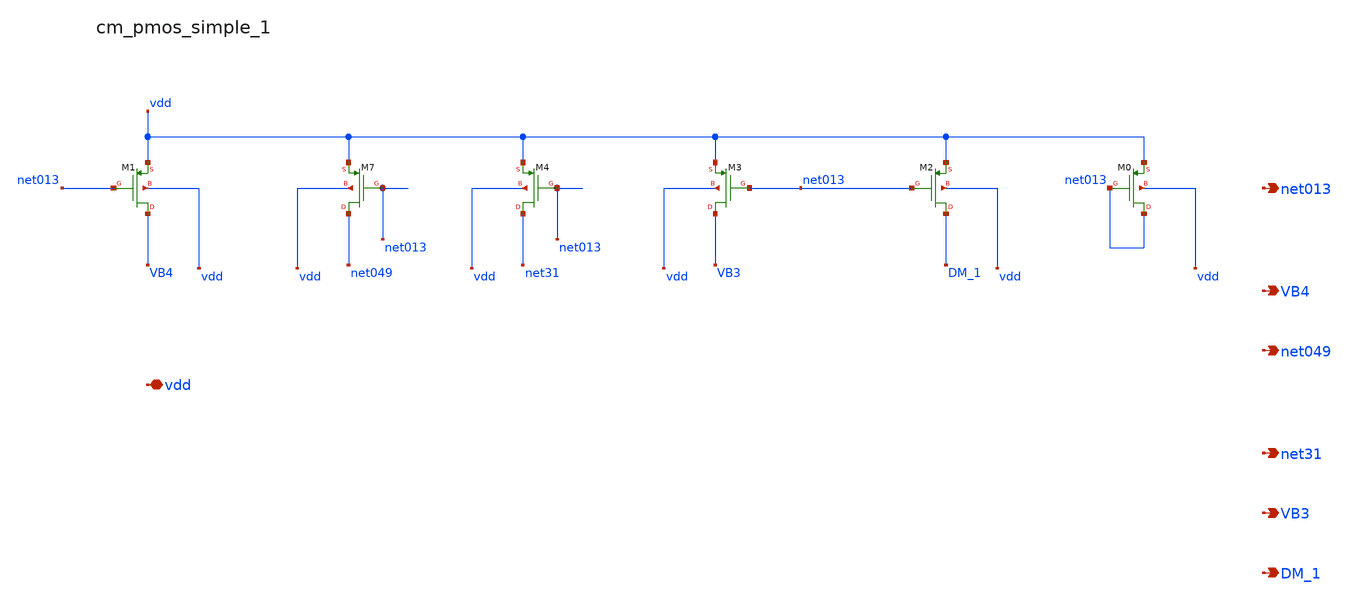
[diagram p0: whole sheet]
** sch_path: analog-db/raw/amp_008_leung_nmcf/hier/blocks/cm_pmos_simple_1.sch
**.subckt cm_pmos_simple_1 vdd net013 VB4 net049 net31 VB3 DM_1
*.iopin vdd
*.opin net013
*.opin VB4
*.opin net049
*.opin net31
*.opin VB3
*.opin DM_1
XM0 net013 net013 vdd vdd sg13_lv_pmos w=x_dut_xm0_w l=x_dut_xm0_l ng=1 m=x_dut_xm0_m
XM1 VB4 net013 vdd vdd sg13_lv_pmos w=x_dut_xm1_w l=x_dut_xm1_l ng=1 m=x_dut_xm1_m
XM2 DM_1 net013 vdd vdd sg13_lv_pmos w=x_dut_xm2_w l=x_dut_xm2_l ng=1 m=x_dut_xm2_m
XM3 VB3 net013 vdd vdd sg13_lv_pmos w=x_dut_xm3_w l=x_dut_xm3_l ng=1 m=x_dut_xm3_m
XM4 net31 net013 vdd vdd sg13_lv_pmos w=x_dut_xm4_w l=x_dut_xm4_l ng=1 m=x_dut_xm4_m
XM7 net049 net013 vdd vdd sg13_lv_pmos w=x_dut_xm7_w l=x_dut_xm7_l ng=1 m=x_dut_xm7_m
**.ends
.end
